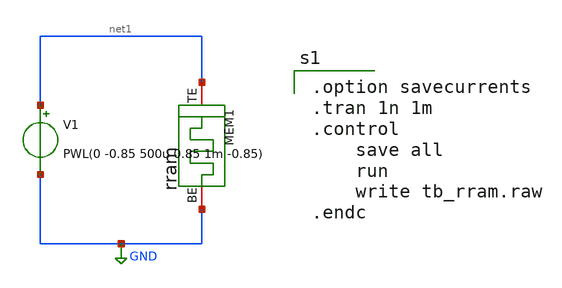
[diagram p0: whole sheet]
** sch_path: designs/tb_memristor/tb_rram.sch
**.subckt tb_rram
MEM1 net1 GND rram
V1 net1 GND PWL(0 -0.85 500u 0.85 1m -0.85)
.save i(v1)
**** begin user architecture code

.option savecurrents
.tran 1n 1m
.control
	save all
	run
	write tb_rram.raw
.endc

 ** opencircuitdesign pdks install
*.inc /foss/designs/spike_130/designs/memristors/rram_v0/rram.spice
.inc $PDK_ROOT/sky130A/libs.tech/ngspice/rram.spice
*.inc $::SKYWATER_MODELS/rram.spice
**** end user architecture code
**.ends
.GLOBAL GND
.end
